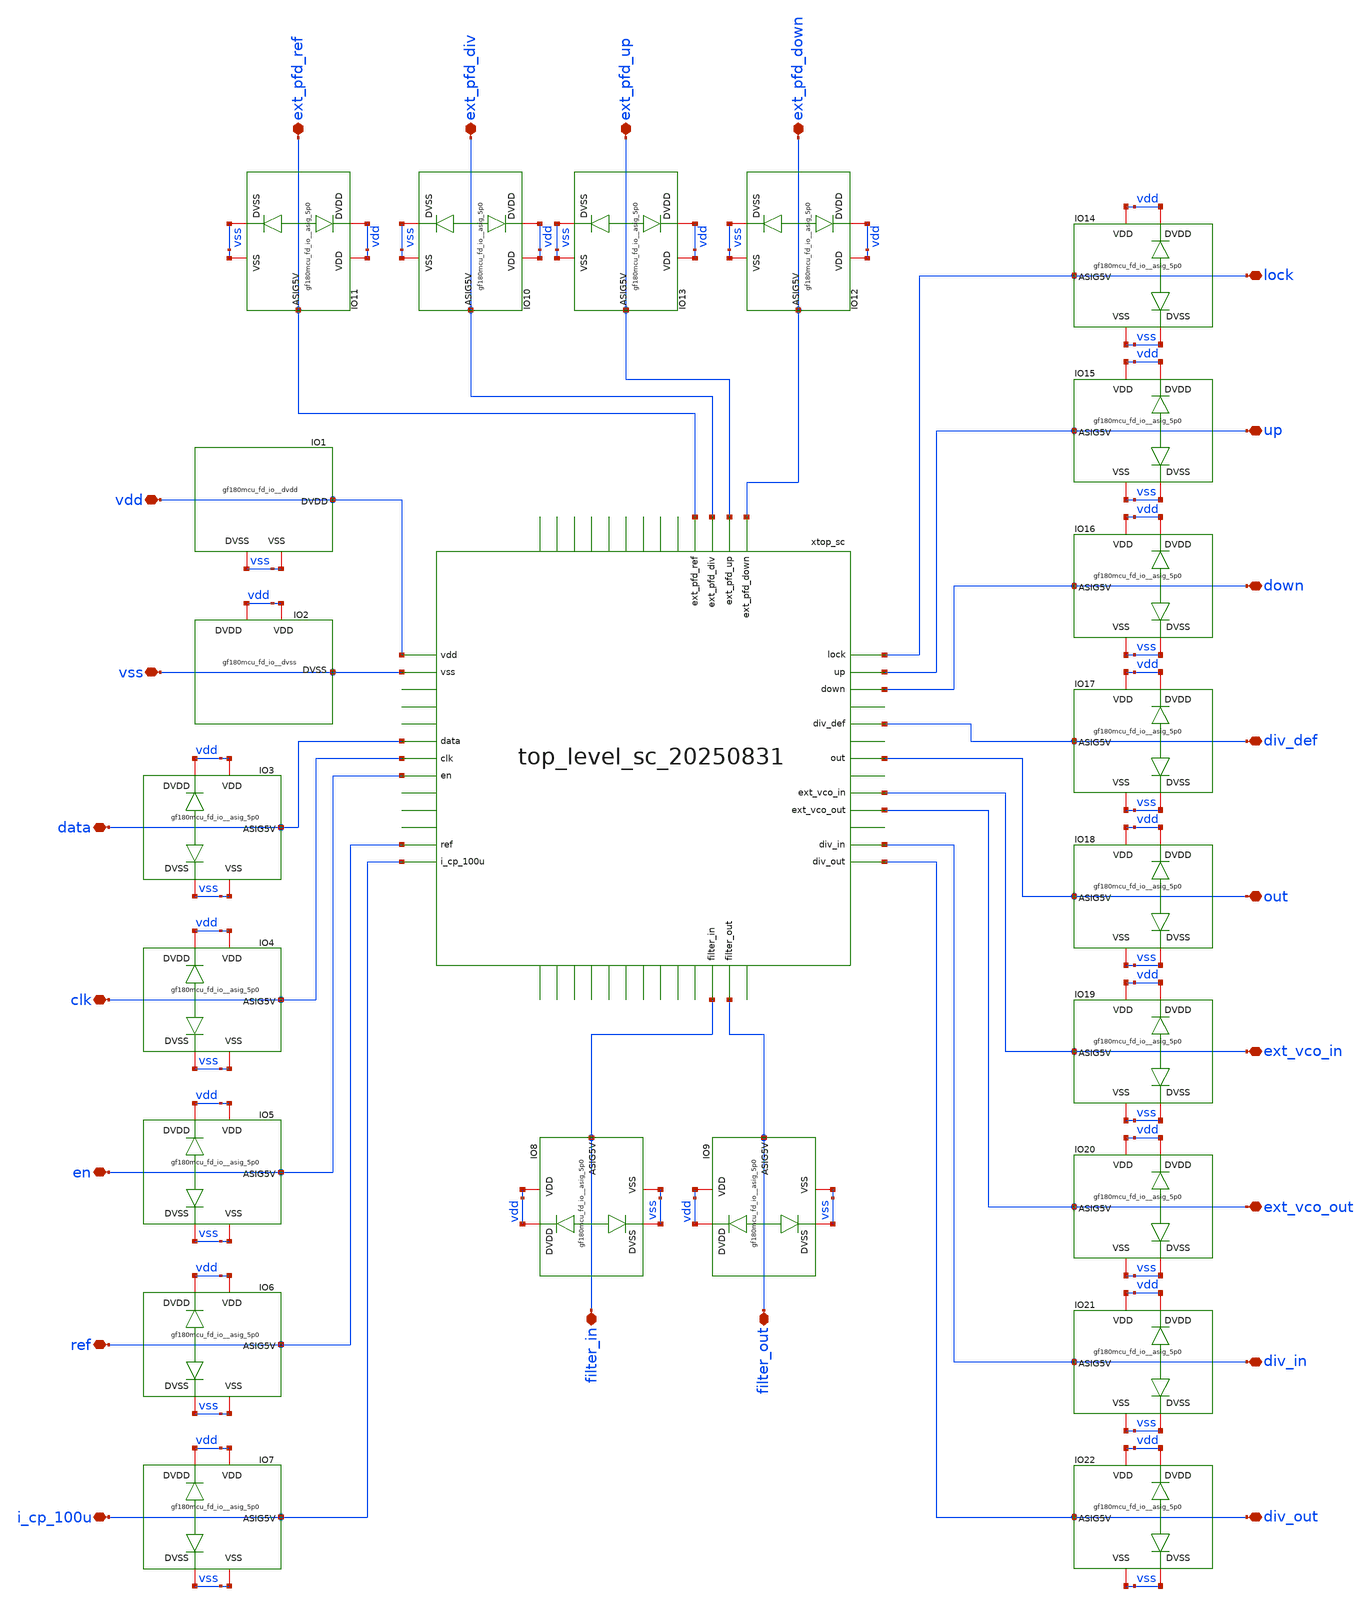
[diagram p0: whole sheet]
** sch_path: designs/libs/top_level/top_level_20250831/top_level_die_20250831/top_level_die_20250831.sch
**.subckt top_level_die_20250831 vdd vss ref i_cp_100u filter_in filter_out ext_pfd_ref ext_pfd_up
*+ ext_pfd_down ext_pfd_div up down out lock ext_vco_out ext_vco_in div_out div_in div_def data clk en
*.iopin vdd
*.iopin vss
*.iopin ref
*.iopin i_cp_100u
*.iopin filter_in
*.iopin filter_out
*.iopin ext_pfd_ref
*.iopin ext_pfd_up
*.iopin ext_pfd_down
*.iopin ext_pfd_div
*.iopin up
*.iopin down
*.iopin out
*.iopin lock
*.iopin ext_vco_out
*.iopin ext_vco_in
*.iopin div_out
*.iopin div_in
*.iopin div_def
*.iopin data
*.iopin clk
*.iopin en
xtop_sc vdd vss data clk en ref i_cp_100u ext_pfd_ref ext_pfd_div ext_pfd_up ext_pfd_down lock up
+ down filter_out ext_vco_in div_in div_out out filter_in ext_vco_out div_def top_level_sc_20250831
XIO1 vdd vss vss gf180mcu_fd_io__dvdd
XIO2 vdd vss vdd gf180mcu_fd_io__dvss
XIO3 data vdd vss vdd vss gf180mcu_fd_io__asig_5p0
XIO4 clk vdd vss vdd vss gf180mcu_fd_io__asig_5p0
XIO5 en vdd vss vdd vss gf180mcu_fd_io__asig_5p0
XIO6 ref vdd vss vdd vss gf180mcu_fd_io__asig_5p0
XIO7 i_cp_100u vdd vss vdd vss gf180mcu_fd_io__asig_5p0
XIO8 filter_in vdd vss vdd vss gf180mcu_fd_io__asig_5p0
XIO9 filter_out vdd vss vdd vss gf180mcu_fd_io__asig_5p0
XIO10 ext_pfd_div vdd vss vdd vss gf180mcu_fd_io__asig_5p0
XIO11 ext_pfd_ref vdd vss vdd vss gf180mcu_fd_io__asig_5p0
XIO12 ext_pfd_down vdd vss vdd vss gf180mcu_fd_io__asig_5p0
XIO13 ext_pfd_up vdd vss vdd vss gf180mcu_fd_io__asig_5p0
XIO14 lock vdd vss vdd vss gf180mcu_fd_io__asig_5p0
XIO15 up vdd vss vdd vss gf180mcu_fd_io__asig_5p0
XIO16 down vdd vss vdd vss gf180mcu_fd_io__asig_5p0
XIO17 div_def vdd vss vdd vss gf180mcu_fd_io__asig_5p0
XIO18 out vdd vss vdd vss gf180mcu_fd_io__asig_5p0
XIO19 ext_vco_in vdd vss vdd vss gf180mcu_fd_io__asig_5p0
XIO20 ext_vco_out vdd vss vdd vss gf180mcu_fd_io__asig_5p0
XIO21 div_in vdd vss vdd vss gf180mcu_fd_io__asig_5p0
XIO22 div_out vdd vss vdd vss gf180mcu_fd_io__asig_5p0
**.ends
.end
